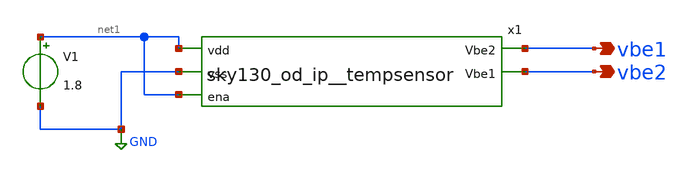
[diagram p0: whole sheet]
** sch_path: xschem/sky130_od_ip__tempsensor_tb.sch
**.subckt sky130_od_ip__tempsensor_tb vbe1 vbe2
*.opin vbe1
*.opin vbe2
V1 net1 GND 1.8
x1 net1 GND vbe1 vbe2 net1 sky130_od_ip__tempsensor
**** begin user architecture code

.lib /usr/local/share/pdk/sky130A/libs.tech/ngspice/sky130.lib.spice tt


.control
dc temp -40 125 10
plot V(vbe1) V(vbe2)-V(vbe1) V(vbe1)+10.3766*(V(vbe2)-V(vbe1))
plot 10.3766/(10.3766+V(vbe1)/(V(vbe2)-V(vbe1)))
.endc

**** end user architecture code
**.ends
.GLOBAL GND
.end
